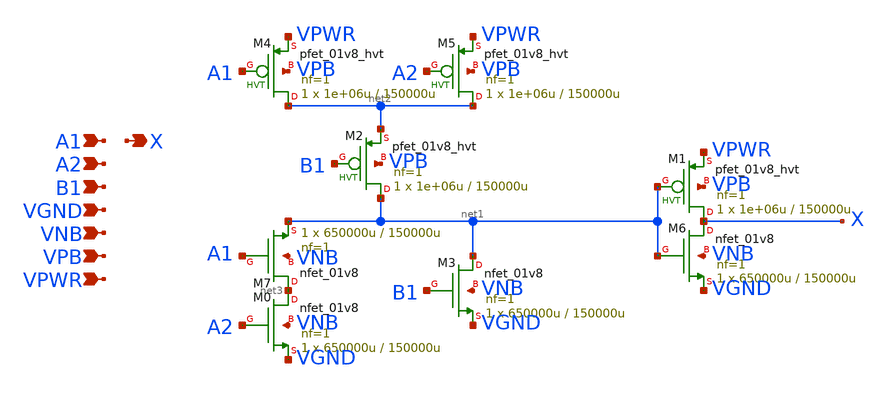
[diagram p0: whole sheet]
** sch_path: schematics/a21o/sky130_fd_sc_hd__a21o_1.sch
**.subckt sky130_fd_sc_hd__a21o_1 A1 A2 B1 VGND VNB VPB VPWR X
*.ipin A1
*.ipin A2
*.ipin B1
*.ipin VGND
*.ipin VNB
*.ipin VPB
*.ipin VPWR
*.opin X
XM1 X net1 VPWR VPB sky130_fd_pr__pfet_01v8_hvt L=150000u W=1e+06u nf=1 ad='int((1 + 1)/2) * 1e+06u / 1 * 0.29'
+ as='int((1 + 2)/2) * 1e+06u / 1 * 0.29' pd='2*int((1 + 1)/2) * (1e+06u / 1 + 0.29)' ps='2*int((1 + 2)/2) * (1e+06u / 1 + 0.29)'
+ nrd='0.29 / 1e+06u ' nrs='0.29 / 1e+06u ' sa=0 sb=0 sd=0 mult=1 m=1
XM6 X net1 VGND VNB sky130_fd_pr__nfet_01v8 L=150000u W=650000u nf=1 ad='int((1 + 1)/2) * 650000u / 1 * 0.29'
+ as='int((1 + 2)/2) * 650000u / 1 * 0.29' pd='2*int((1 + 1)/2) * (650000u / 1 + 0.29)' ps='2*int((1 + 2)/2) * (650000u / 1 + 0.29)'
+ nrd='0.29 / 650000u ' nrs='0.29 / 650000u ' sa=0 sb=0 sd=0 mult=1 m=1
XM4 net2 A1 VPWR VPB sky130_fd_pr__pfet_01v8_hvt L=150000u W=1e+06u nf=1 ad='int((1 + 1)/2) * 1e+06u / 1 * 0.29'
+ as='int((1 + 2)/2) * 1e+06u / 1 * 0.29' pd='2*int((1 + 1)/2) * (1e+06u / 1 + 0.29)' ps='2*int((1 + 2)/2) * (1e+06u / 1 + 0.29)'
+ nrd='0.29 / 1e+06u ' nrs='0.29 / 1e+06u ' sa=0 sb=0 sd=0 mult=1 m=1
XM5 net2 A2 VPWR VPB sky130_fd_pr__pfet_01v8_hvt L=150000u W=1e+06u nf=1 ad='int((1 + 1)/2) * 1e+06u / 1 * 0.29'
+ as='int((1 + 2)/2) * 1e+06u / 1 * 0.29' pd='2*int((1 + 1)/2) * (1e+06u / 1 + 0.29)' ps='2*int((1 + 2)/2) * (1e+06u / 1 + 0.29)'
+ nrd='0.29 / 1e+06u ' nrs='0.29 / 1e+06u ' sa=0 sb=0 sd=0 mult=1 m=1
XM2 net1 B1 net2 VPB sky130_fd_pr__pfet_01v8_hvt L=150000u W=1e+06u nf=1 ad='int((1 + 1)/2) * 1e+06u / 1 * 0.29'
+ as='int((1 + 2)/2) * 1e+06u / 1 * 0.29' pd='2*int((1 + 1)/2) * (1e+06u / 1 + 0.29)' ps='2*int((1 + 2)/2) * (1e+06u / 1 + 0.29)'
+ nrd='0.29 / 1e+06u ' nrs='0.29 / 1e+06u ' sa=0 sb=0 sd=0 mult=1 m=1
XM7 net3 A1 net1 VNB sky130_fd_pr__nfet_01v8 L=150000u W=650000u nf=1 ad='int((1 + 1)/2) * 650000u / 1 * 0.29'
+ as='int((1 + 2)/2) * 650000u / 1 * 0.29' pd='2*int((1 + 1)/2) * (650000u / 1 + 0.29)' ps='2*int((1 + 2)/2) * (650000u / 1 + 0.29)'
+ nrd='0.29 / 650000u ' nrs='0.29 / 650000u ' sa=0 sb=0 sd=0 mult=1 m=1
XM0 net3 A2 VGND VNB sky130_fd_pr__nfet_01v8 L=150000u W=650000u nf=1 ad='int((1 + 1)/2) * 650000u / 1 * 0.29'
+ as='int((1 + 2)/2) * 650000u / 1 * 0.29' pd='2*int((1 + 1)/2) * (650000u / 1 + 0.29)' ps='2*int((1 + 2)/2) * (650000u / 1 + 0.29)'
+ nrd='0.29 / 650000u ' nrs='0.29 / 650000u ' sa=0 sb=0 sd=0 mult=1 m=1
XM3 net1 B1 VGND VNB sky130_fd_pr__nfet_01v8 L=150000u W=650000u nf=1 ad='int((1 + 1)/2) * 650000u / 1 * 0.29'
+ as='int((1 + 2)/2) * 650000u / 1 * 0.29' pd='2*int((1 + 1)/2) * (650000u / 1 + 0.29)' ps='2*int((1 + 2)/2) * (650000u / 1 + 0.29)'
+ nrd='0.29 / 650000u ' nrs='0.29 / 650000u ' sa=0 sb=0 sd=0 mult=1 m=1
**.ends
.end
